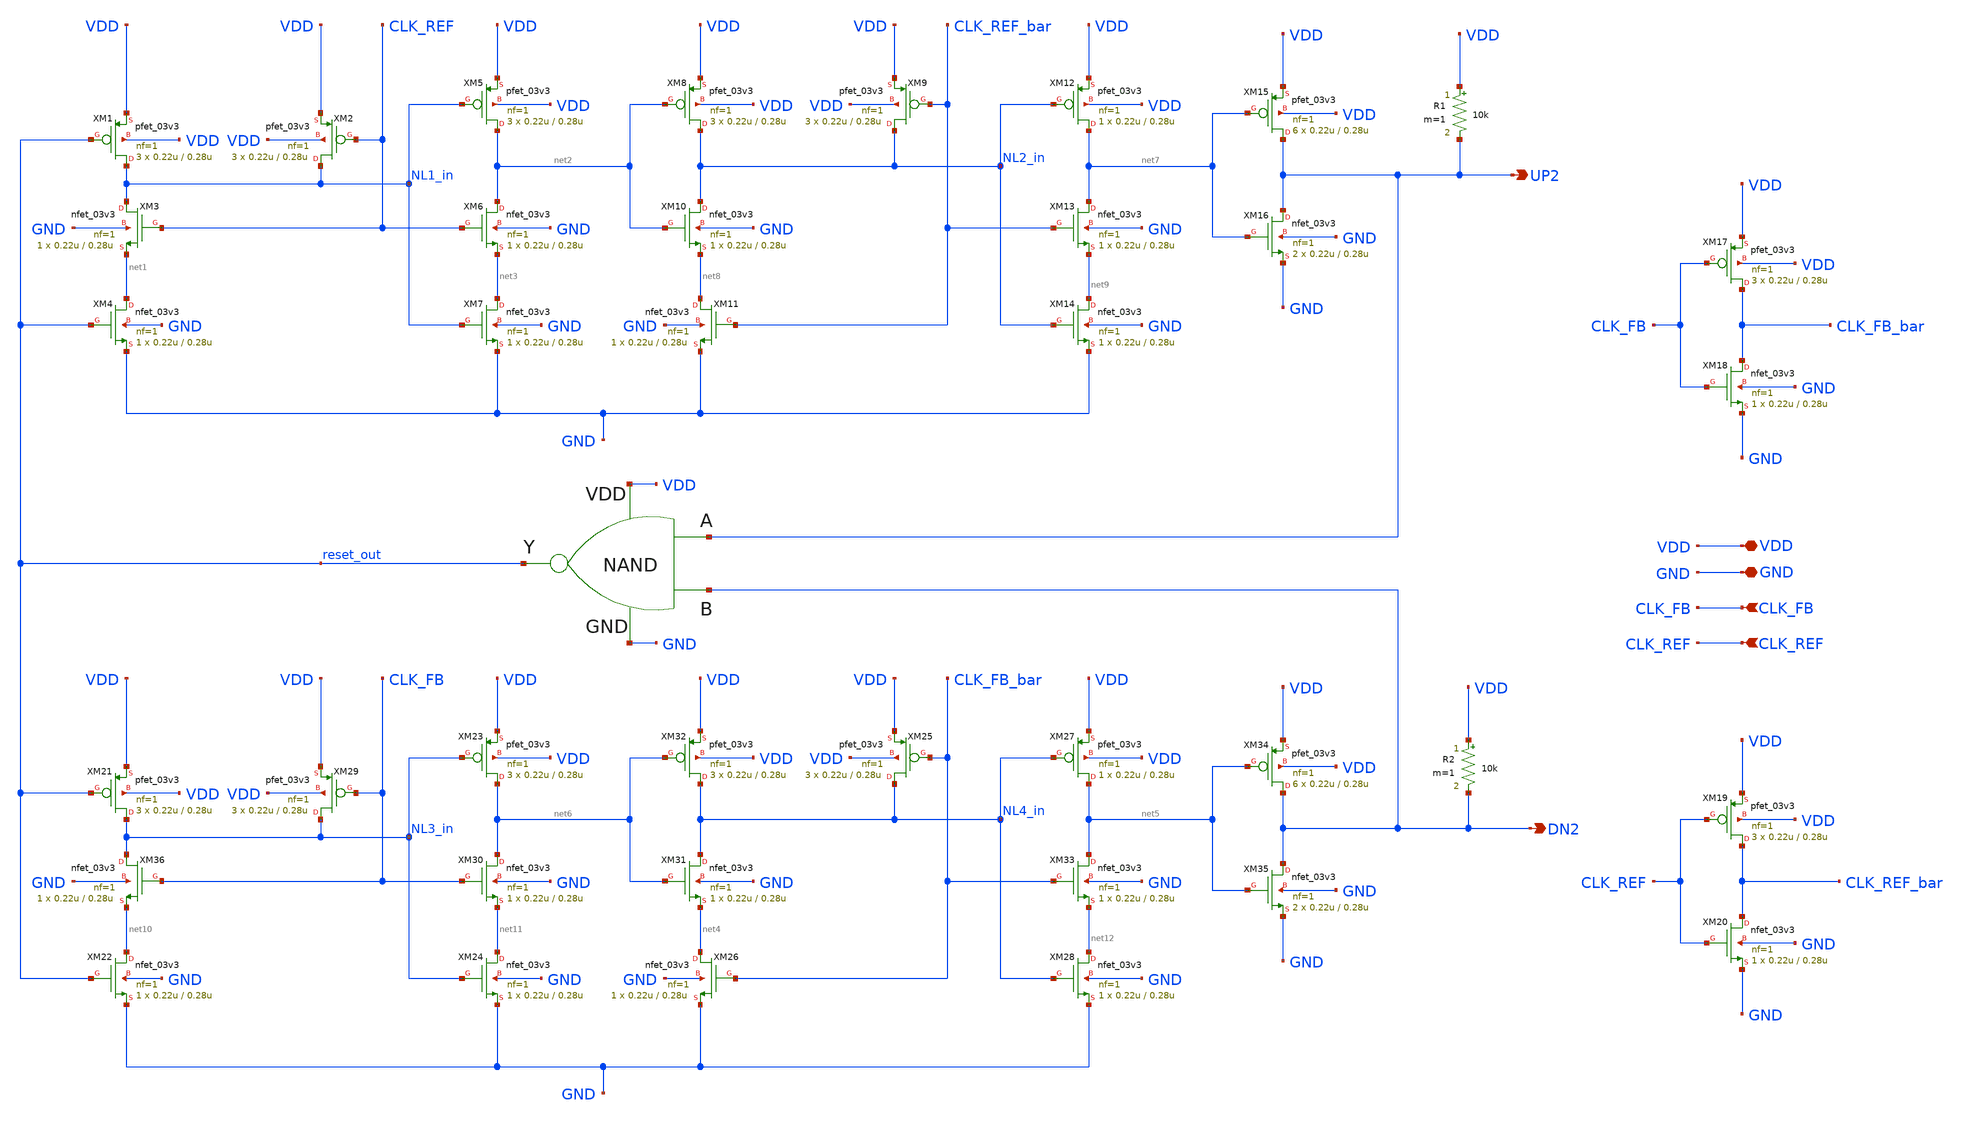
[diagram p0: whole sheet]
** sch_path: PFD/OPL_PFD.sch
**.subckt OPL_PFD UP2 CLK_FB CLK_REF DN2 VDD GND
*.opin UP2
*.ipin CLK_FB
*.ipin CLK_REF
*.opin DN2
*.iopin VDD
*.iopin GND
XM1 NL1_in reset_out VDD VDD pfet_03v3 L=0.28u W=0.22u nf=1 ad='int((nf+1)/2) * W/nf * 0.18u' as='int((nf+2)/2) * W/nf * 0.18u'
+ pd='2*int((nf+1)/2) * (W/nf + 0.18u)' ps='2*int((nf+2)/2) * (W/nf + 0.18u)' nrd='0.18u / W' nrs='0.18u / W'
+ sa=0 sb=0 sd=0 m=3
XM4 net1 reset_out GND GND nfet_03v3 L=0.28u W=0.22u nf=1 ad='int((nf+1)/2) * W/nf * 0.18u' as='int((nf+2)/2) * W/nf * 0.18u'
+ pd='2*int((nf+1)/2) * (W/nf + 0.18u)' ps='2*int((nf+2)/2) * (W/nf + 0.18u)' nrd='0.18u / W' nrs='0.18u / W'
+ sa=0 sb=0 sd=0 m=1
XM5 net2 NL1_in VDD VDD pfet_03v3 L=0.28u W=0.22u nf=1 ad='int((nf+1)/2) * W/nf * 0.18u' as='int((nf+2)/2) * W/nf * 0.18u'
+ pd='2*int((nf+1)/2) * (W/nf + 0.18u)' ps='2*int((nf+2)/2) * (W/nf + 0.18u)' nrd='0.18u / W' nrs='0.18u / W'
+ sa=0 sb=0 sd=0 m=3
XM7 net3 NL1_in GND GND nfet_03v3 L=0.28u W=0.22u nf=1 ad='int((nf+1)/2) * W/nf * 0.18u' as='int((nf+2)/2) * W/nf * 0.18u'
+ pd='2*int((nf+1)/2) * (W/nf + 0.18u)' ps='2*int((nf+2)/2) * (W/nf + 0.18u)' nrd='0.18u / W' nrs='0.18u / W'
+ sa=0 sb=0 sd=0 m=1
XM9 NL2_in CLK_REF_bar VDD VDD pfet_03v3 L=0.28u W=0.22u nf=1 ad='int((nf+1)/2) * W/nf * 0.18u' as='int((nf+2)/2) * W/nf * 0.18u'
+ pd='2*int((nf+1)/2) * (W/nf + 0.18u)' ps='2*int((nf+2)/2) * (W/nf + 0.18u)' nrd='0.18u / W' nrs='0.18u / W'
+ sa=0 sb=0 sd=0 m=3
XM11 net8 CLK_REF_bar GND GND nfet_03v3 L=0.28u W=0.22u nf=1 ad='int((nf+1)/2) * W/nf * 0.18u' as='int((nf+2)/2) * W/nf * 0.18u'
+ pd='2*int((nf+1)/2) * (W/nf + 0.18u)' ps='2*int((nf+2)/2) * (W/nf + 0.18u)' nrd='0.18u / W' nrs='0.18u / W'
+ sa=0 sb=0 sd=0 m=1
XM12 net7 NL2_in VDD VDD pfet_03v3 L=0.28u W=0.22u nf=1 ad='int((nf+1)/2) * W/nf * 0.18u' as='int((nf+2)/2) * W/nf * 0.18u'
+ pd='2*int((nf+1)/2) * (W/nf + 0.18u)' ps='2*int((nf+2)/2) * (W/nf + 0.18u)' nrd='0.18u / W' nrs='0.18u / W'
+ sa=0 sb=0 sd=0 m=1
XM14 net9 NL2_in GND GND nfet_03v3 L=0.28u W=0.22u nf=1 ad='int((nf+1)/2) * W/nf * 0.18u' as='int((nf+2)/2) * W/nf * 0.18u'
+ pd='2*int((nf+1)/2) * (W/nf + 0.18u)' ps='2*int((nf+2)/2) * (W/nf + 0.18u)' nrd='0.18u / W' nrs='0.18u / W'
+ sa=0 sb=0 sd=0 m=1
XM2 NL1_in CLK_REF VDD VDD pfet_03v3 L=0.28u W=0.22u nf=1 ad='int((nf+1)/2) * W/nf * 0.18u' as='int((nf+2)/2) * W/nf * 0.18u'
+ pd='2*int((nf+1)/2) * (W/nf + 0.18u)' ps='2*int((nf+2)/2) * (W/nf + 0.18u)' nrd='0.18u / W' nrs='0.18u / W'
+ sa=0 sb=0 sd=0 m=3
XM6 net2 CLK_REF net3 GND nfet_03v3 L=0.28u W=0.22u nf=1 ad='int((nf+1)/2) * W/nf * 0.18u' as='int((nf+2)/2) * W/nf * 0.18u'
+ pd='2*int((nf+1)/2) * (W/nf + 0.18u)' ps='2*int((nf+2)/2) * (W/nf + 0.18u)' nrd='0.18u / W' nrs='0.18u / W'
+ sa=0 sb=0 sd=0 m=1
XM10 NL2_in net2 net8 GND nfet_03v3 L=0.28u W=0.22u nf=1 ad='int((nf+1)/2) * W/nf * 0.18u' as='int((nf+2)/2) * W/nf * 0.18u'
+ pd='2*int((nf+1)/2) * (W/nf + 0.18u)' ps='2*int((nf+2)/2) * (W/nf + 0.18u)' nrd='0.18u / W' nrs='0.18u / W'
+ sa=0 sb=0 sd=0 m=1
XM8 NL2_in net2 VDD VDD pfet_03v3 L=0.28u W=0.22u nf=1 ad='int((nf+1)/2) * W/nf * 0.18u' as='int((nf+2)/2) * W/nf * 0.18u'
+ pd='2*int((nf+1)/2) * (W/nf + 0.18u)' ps='2*int((nf+2)/2) * (W/nf + 0.18u)' nrd='0.18u / W' nrs='0.18u / W'
+ sa=0 sb=0 sd=0 m=3
XM13 net7 CLK_REF_bar net9 GND nfet_03v3 L=0.28u W=0.22u nf=1 ad='int((nf+1)/2) * W/nf * 0.18u' as='int((nf+2)/2) * W/nf * 0.18u'
+ pd='2*int((nf+1)/2) * (W/nf + 0.18u)' ps='2*int((nf+2)/2) * (W/nf + 0.18u)' nrd='0.18u / W' nrs='0.18u / W'
+ sa=0 sb=0 sd=0 m=1
XM15 UP2 net7 VDD VDD pfet_03v3 L=0.28u W=0.22u nf=1 ad='int((nf+1)/2) * W/nf * 0.18u' as='int((nf+2)/2) * W/nf * 0.18u'
+ pd='2*int((nf+1)/2) * (W/nf + 0.18u)' ps='2*int((nf+2)/2) * (W/nf + 0.18u)' nrd='0.18u / W' nrs='0.18u / W'
+ sa=0 sb=0 sd=0 m=6
XM16 UP2 net7 GND GND nfet_03v3 L=0.28u W=0.22u nf=1 ad='int((nf+1)/2) * W/nf * 0.18u' as='int((nf+2)/2) * W/nf * 0.18u'
+ pd='2*int((nf+1)/2) * (W/nf + 0.18u)' ps='2*int((nf+2)/2) * (W/nf + 0.18u)' nrd='0.18u / W' nrs='0.18u / W'
+ sa=0 sb=0 sd=0 m=2
XM17 CLK_FB_bar CLK_FB VDD VDD pfet_03v3 L=0.28u W=0.22u nf=1 ad='int((nf+1)/2) * W/nf * 0.18u' as='int((nf+2)/2) * W/nf * 0.18u'
+ pd='2*int((nf+1)/2) * (W/nf + 0.18u)' ps='2*int((nf+2)/2) * (W/nf + 0.18u)' nrd='0.18u / W' nrs='0.18u / W'
+ sa=0 sb=0 sd=0 m=3
XM18 CLK_FB_bar CLK_FB GND GND nfet_03v3 L=0.28u W=0.22u nf=1 ad='int((nf+1)/2) * W/nf * 0.18u' as='int((nf+2)/2) * W/nf * 0.18u'
+ pd='2*int((nf+1)/2) * (W/nf + 0.18u)' ps='2*int((nf+2)/2) * (W/nf + 0.18u)' nrd='0.18u / W' nrs='0.18u / W'
+ sa=0 sb=0 sd=0 m=1
XM19 CLK_REF_bar CLK_REF VDD VDD pfet_03v3 L=0.28u W=0.22u nf=1 ad='int((nf+1)/2) * W/nf * 0.18u' as='int((nf+2)/2) * W/nf * 0.18u'
+ pd='2*int((nf+1)/2) * (W/nf + 0.18u)' ps='2*int((nf+2)/2) * (W/nf + 0.18u)' nrd='0.18u / W' nrs='0.18u / W'
+ sa=0 sb=0 sd=0 m=3
XM20 CLK_REF_bar CLK_REF GND GND nfet_03v3 L=0.28u W=0.22u nf=1 ad='int((nf+1)/2) * W/nf * 0.18u' as='int((nf+2)/2) * W/nf * 0.18u'
+ pd='2*int((nf+1)/2) * (W/nf + 0.18u)' ps='2*int((nf+2)/2) * (W/nf + 0.18u)' nrd='0.18u / W' nrs='0.18u / W'
+ sa=0 sb=0 sd=0 m=1
XM3 NL1_in CLK_REF net1 GND nfet_03v3 L=0.28u W=0.22u nf=1 ad='int((nf+1)/2) * W/nf * 0.18u' as='int((nf+2)/2) * W/nf * 0.18u'
+ pd='2*int((nf+1)/2) * (W/nf + 0.18u)' ps='2*int((nf+2)/2) * (W/nf + 0.18u)' nrd='0.18u / W' nrs='0.18u / W'
+ sa=0 sb=0 sd=0 m=1
XM21 NL3_in reset_out VDD VDD pfet_03v3 L=0.28u W=0.22u nf=1 ad='int((nf+1)/2) * W/nf * 0.18u' as='int((nf+2)/2) * W/nf * 0.18u'
+ pd='2*int((nf+1)/2) * (W/nf + 0.18u)' ps='2*int((nf+2)/2) * (W/nf + 0.18u)' nrd='0.18u / W' nrs='0.18u / W'
+ sa=0 sb=0 sd=0 m=3
XM22 net10 reset_out GND GND nfet_03v3 L=0.28u W=0.22u nf=1 ad='int((nf+1)/2) * W/nf * 0.18u' as='int((nf+2)/2) * W/nf * 0.18u'
+ pd='2*int((nf+1)/2) * (W/nf + 0.18u)' ps='2*int((nf+2)/2) * (W/nf + 0.18u)' nrd='0.18u / W' nrs='0.18u / W'
+ sa=0 sb=0 sd=0 m=1
XM23 net6 NL3_in VDD VDD pfet_03v3 L=0.28u W=0.22u nf=1 ad='int((nf+1)/2) * W/nf * 0.18u' as='int((nf+2)/2) * W/nf * 0.18u'
+ pd='2*int((nf+1)/2) * (W/nf + 0.18u)' ps='2*int((nf+2)/2) * (W/nf + 0.18u)' nrd='0.18u / W' nrs='0.18u / W'
+ sa=0 sb=0 sd=0 m=3
XM24 net11 NL3_in GND GND nfet_03v3 L=0.28u W=0.22u nf=1 ad='int((nf+1)/2) * W/nf * 0.18u' as='int((nf+2)/2) * W/nf * 0.18u'
+ pd='2*int((nf+1)/2) * (W/nf + 0.18u)' ps='2*int((nf+2)/2) * (W/nf + 0.18u)' nrd='0.18u / W' nrs='0.18u / W'
+ sa=0 sb=0 sd=0 m=1
XM25 NL4_in CLK_FB_bar VDD VDD pfet_03v3 L=0.28u W=0.22u nf=1 ad='int((nf+1)/2) * W/nf * 0.18u' as='int((nf+2)/2) * W/nf * 0.18u'
+ pd='2*int((nf+1)/2) * (W/nf + 0.18u)' ps='2*int((nf+2)/2) * (W/nf + 0.18u)' nrd='0.18u / W' nrs='0.18u / W'
+ sa=0 sb=0 sd=0 m=3
XM26 net4 CLK_FB_bar GND GND nfet_03v3 L=0.28u W=0.22u nf=1 ad='int((nf+1)/2) * W/nf * 0.18u' as='int((nf+2)/2) * W/nf * 0.18u'
+ pd='2*int((nf+1)/2) * (W/nf + 0.18u)' ps='2*int((nf+2)/2) * (W/nf + 0.18u)' nrd='0.18u / W' nrs='0.18u / W'
+ sa=0 sb=0 sd=0 m=1
XM27 net5 NL4_in VDD VDD pfet_03v3 L=0.28u W=0.22u nf=1 ad='int((nf+1)/2) * W/nf * 0.18u' as='int((nf+2)/2) * W/nf * 0.18u'
+ pd='2*int((nf+1)/2) * (W/nf + 0.18u)' ps='2*int((nf+2)/2) * (W/nf + 0.18u)' nrd='0.18u / W' nrs='0.18u / W'
+ sa=0 sb=0 sd=0 m=1
XM28 net12 NL4_in GND GND nfet_03v3 L=0.28u W=0.22u nf=1 ad='int((nf+1)/2) * W/nf * 0.18u' as='int((nf+2)/2) * W/nf * 0.18u'
+ pd='2*int((nf+1)/2) * (W/nf + 0.18u)' ps='2*int((nf+2)/2) * (W/nf + 0.18u)' nrd='0.18u / W' nrs='0.18u / W'
+ sa=0 sb=0 sd=0 m=1
XM29 NL3_in CLK_FB VDD VDD pfet_03v3 L=0.28u W=0.22u nf=1 ad='int((nf+1)/2) * W/nf * 0.18u' as='int((nf+2)/2) * W/nf * 0.18u'
+ pd='2*int((nf+1)/2) * (W/nf + 0.18u)' ps='2*int((nf+2)/2) * (W/nf + 0.18u)' nrd='0.18u / W' nrs='0.18u / W'
+ sa=0 sb=0 sd=0 m=3
XM30 net6 CLK_FB net11 GND nfet_03v3 L=0.28u W=0.22u nf=1 ad='int((nf+1)/2) * W/nf * 0.18u' as='int((nf+2)/2) * W/nf * 0.18u'
+ pd='2*int((nf+1)/2) * (W/nf + 0.18u)' ps='2*int((nf+2)/2) * (W/nf + 0.18u)' nrd='0.18u / W' nrs='0.18u / W'
+ sa=0 sb=0 sd=0 m=1
XM31 NL4_in net6 net4 GND nfet_03v3 L=0.28u W=0.22u nf=1 ad='int((nf+1)/2) * W/nf * 0.18u' as='int((nf+2)/2) * W/nf * 0.18u'
+ pd='2*int((nf+1)/2) * (W/nf + 0.18u)' ps='2*int((nf+2)/2) * (W/nf + 0.18u)' nrd='0.18u / W' nrs='0.18u / W'
+ sa=0 sb=0 sd=0 m=1
XM32 NL4_in net6 VDD VDD pfet_03v3 L=0.28u W=0.22u nf=1 ad='int((nf+1)/2) * W/nf * 0.18u' as='int((nf+2)/2) * W/nf * 0.18u'
+ pd='2*int((nf+1)/2) * (W/nf + 0.18u)' ps='2*int((nf+2)/2) * (W/nf + 0.18u)' nrd='0.18u / W' nrs='0.18u / W'
+ sa=0 sb=0 sd=0 m=3
XM33 net5 CLK_FB_bar net12 GND nfet_03v3 L=0.28u W=0.22u nf=1 ad='int((nf+1)/2) * W/nf * 0.18u' as='int((nf+2)/2) * W/nf * 0.18u'
+ pd='2*int((nf+1)/2) * (W/nf + 0.18u)' ps='2*int((nf+2)/2) * (W/nf + 0.18u)' nrd='0.18u / W' nrs='0.18u / W'
+ sa=0 sb=0 sd=0 m=1
XM34 DN2 net5 VDD VDD pfet_03v3 L=0.28u W=0.22u nf=1 ad='int((nf+1)/2) * W/nf * 0.18u' as='int((nf+2)/2) * W/nf * 0.18u'
+ pd='2*int((nf+1)/2) * (W/nf + 0.18u)' ps='2*int((nf+2)/2) * (W/nf + 0.18u)' nrd='0.18u / W' nrs='0.18u / W'
+ sa=0 sb=0 sd=0 m=6
XM35 DN2 net5 GND GND nfet_03v3 L=0.28u W=0.22u nf=1 ad='int((nf+1)/2) * W/nf * 0.18u' as='int((nf+2)/2) * W/nf * 0.18u'
+ pd='2*int((nf+1)/2) * (W/nf + 0.18u)' ps='2*int((nf+2)/2) * (W/nf + 0.18u)' nrd='0.18u / W' nrs='0.18u / W'
+ sa=0 sb=0 sd=0 m=2
XM36 NL3_in CLK_FB net10 GND nfet_03v3 L=0.28u W=0.22u nf=1 ad='int((nf+1)/2) * W/nf * 0.18u' as='int((nf+2)/2) * W/nf * 0.18u'
+ pd='2*int((nf+1)/2) * (W/nf + 0.18u)' ps='2*int((nf+2)/2) * (W/nf + 0.18u)' nrd='0.18u / W' nrs='0.18u / W'
+ sa=0 sb=0 sd=0 m=1
x1 GND UP2 DN2 VDD reset_out NAND
R1 VDD UP2 10k m=1
R2 VDD DN2 10k m=1
**.ends

* expanding   symbol:  NAND.sym # of pins=5
** sym_path: PFD/NAND.sym
** sch_path: PFD/NAND.sch
.subckt NAND GND A B VDD Y
*.opin Y
*.ipin GND
*.ipin VDD
*.ipin A
*.ipin B
XM1 Y A VDD VDD pfet_03v3 L=0.28u W=0.22u nf=1 ad='int((nf+1)/2) * W/nf * 0.18u' as='int((nf+2)/2) * W/nf * 0.18u'
+ pd='2*int((nf+1)/2) * (W/nf + 0.18u)' ps='2*int((nf+2)/2) * (W/nf + 0.18u)' nrd='0.18u / W' nrs='0.18u / W'
+ sa=0 sb=0 sd=0 m=3
XM3 Y A net1 GND nfet_03v3 L=0.28u W=0.22u nf=1 ad='int((nf+1)/2) * W/nf * 0.18u' as='int((nf+2)/2) * W/nf * 0.18u'
+ pd='2*int((nf+1)/2) * (W/nf + 0.18u)' ps='2*int((nf+2)/2) * (W/nf + 0.18u)' nrd='0.18u / W' nrs='0.18u / W'
+ sa=0 sb=0 sd=0 m=1
XM4 net1 B GND GND nfet_03v3 L=0.28u W=0.22u nf=1 ad='int((nf+1)/2) * W/nf * 0.18u' as='int((nf+2)/2) * W/nf * 0.18u'
+ pd='2*int((nf+1)/2) * (W/nf + 0.18u)' ps='2*int((nf+2)/2) * (W/nf + 0.18u)' nrd='0.18u / W' nrs='0.18u / W'
+ sa=0 sb=0 sd=0 m=1
XM2 Y B VDD VDD pfet_03v3 L=0.28u W=0.22u nf=1 ad='int((nf+1)/2) * W/nf * 0.18u' as='int((nf+2)/2) * W/nf * 0.18u'
+ pd='2*int((nf+1)/2) * (W/nf + 0.18u)' ps='2*int((nf+2)/2) * (W/nf + 0.18u)' nrd='0.18u / W' nrs='0.18u / W'
+ sa=0 sb=0 sd=0 m=3
.ends

.end
